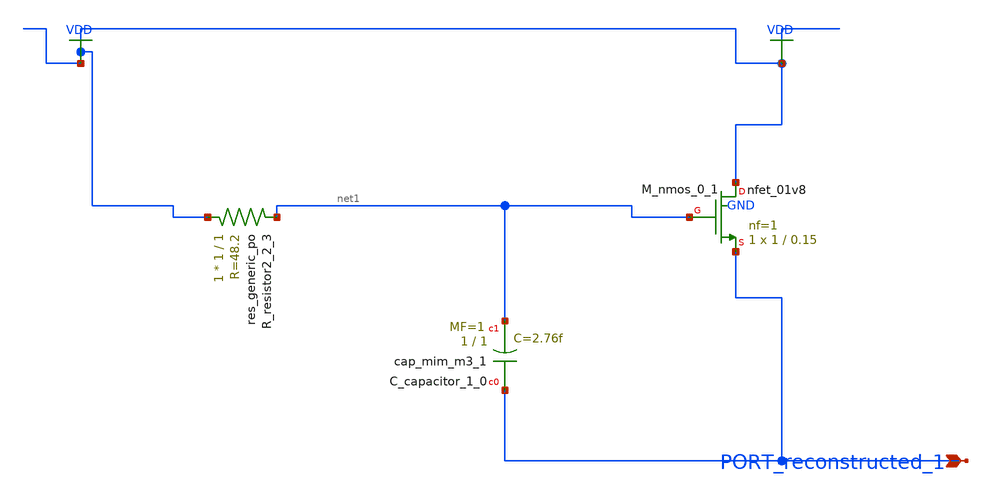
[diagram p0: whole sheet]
** sch_path: schematics/AMSNet/376.sch
**.subckt 376 PORT_reconstructed_1
*.ipin PORT_reconstructed_1
XC_capacitor_1_0 PORT_reconstructed_1 net1 sky130_fd_pr__cap_mim_m3_1 W=1 L=1 MF=1 m=1
XM_nmos_0_1 VDD net1 PORT_reconstructed_1 GND sky130_fd_pr__nfet_01v8 L=0.15 W=1 nf=1 ad='int((1 + 1)/2) * 1 / 1 * 0.29'
+ as='int((1 + 2)/2) * 1 / 1 * 0.29' pd='2*int((1 + 1)/2) * (1 / 1 + 0.29)' ps='2*int((1 + 2)/2) * (1 / 1 + 0.29)'
+ nrd='0.29 / 1 ' nrs='0.29 / 1 ' sa=0 sb=0 sd=0 mult=1 m=1
XR_resistor2_2_3 VDD net1 sky130_fd_pr__res_generic_po W=1 L=1 m=1
**.ends
.GLOBAL VDD
.end
